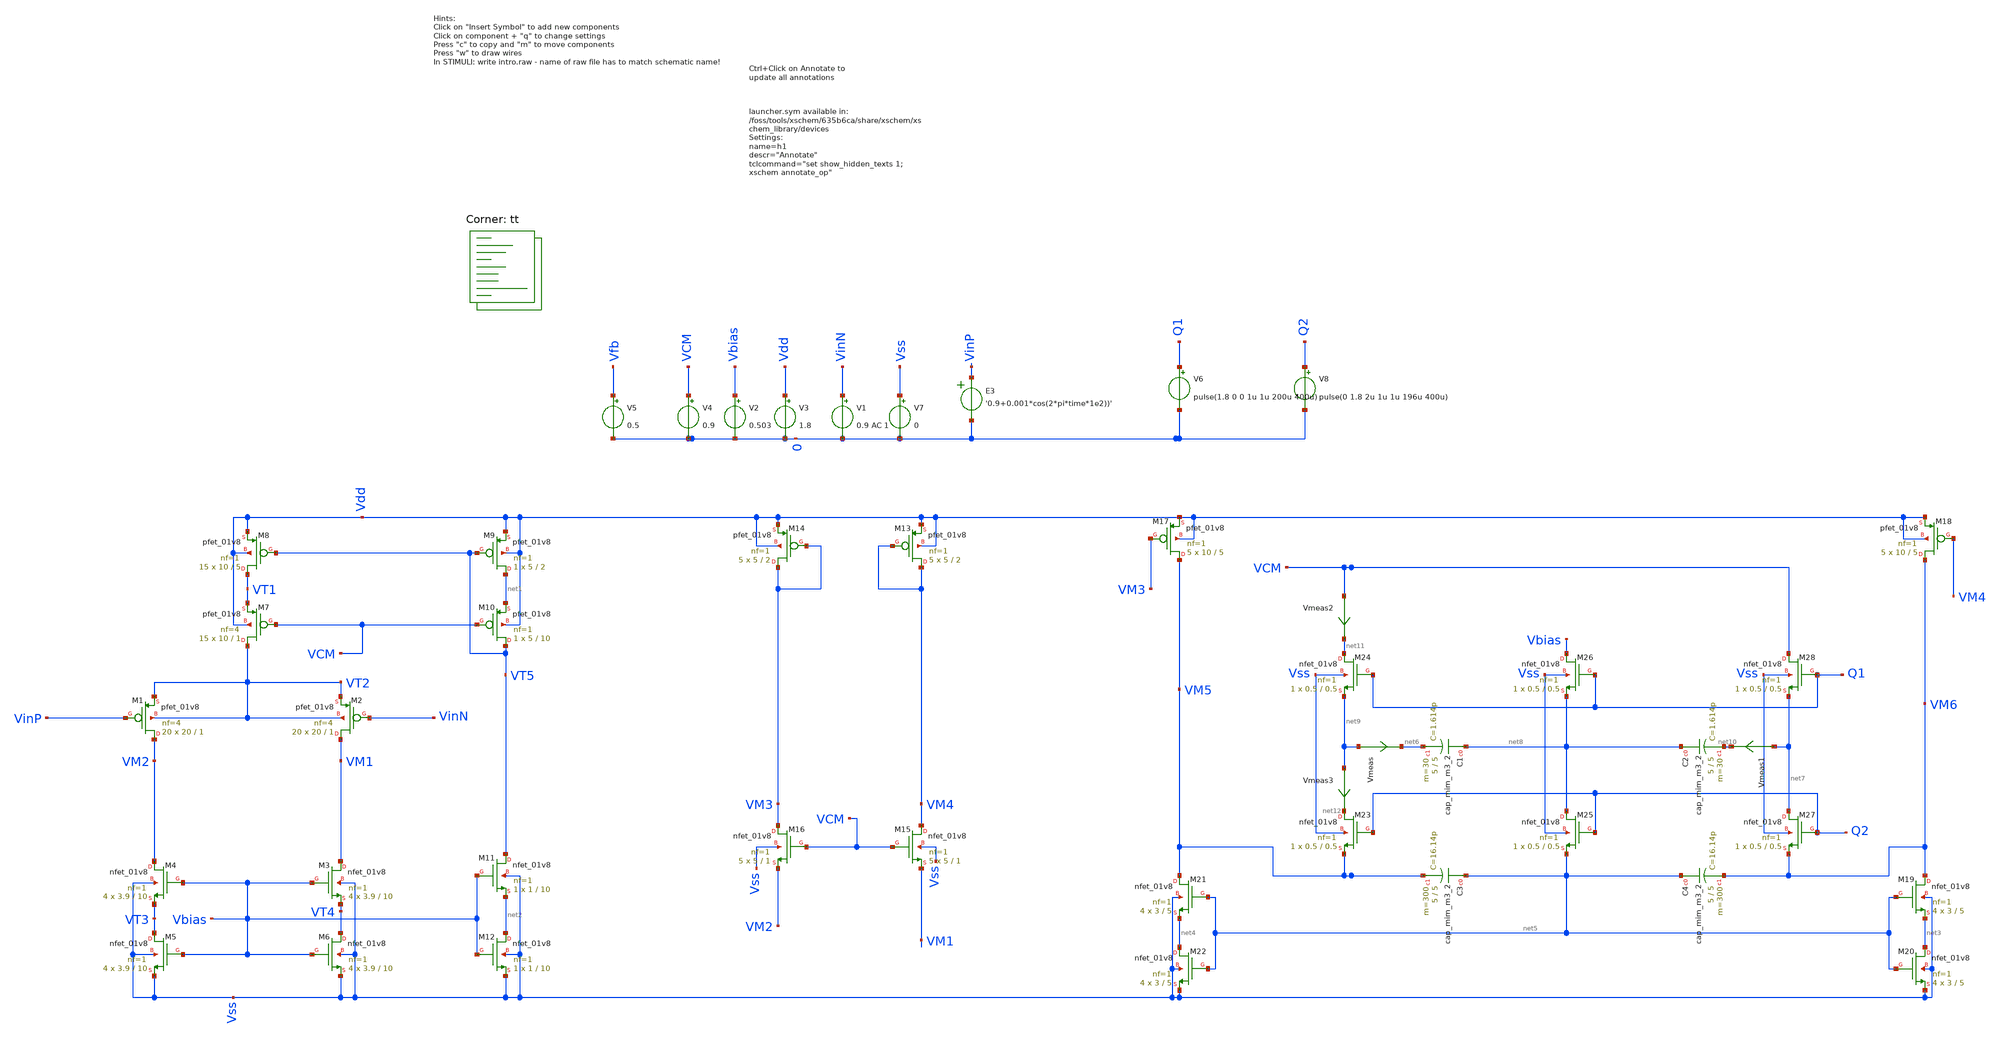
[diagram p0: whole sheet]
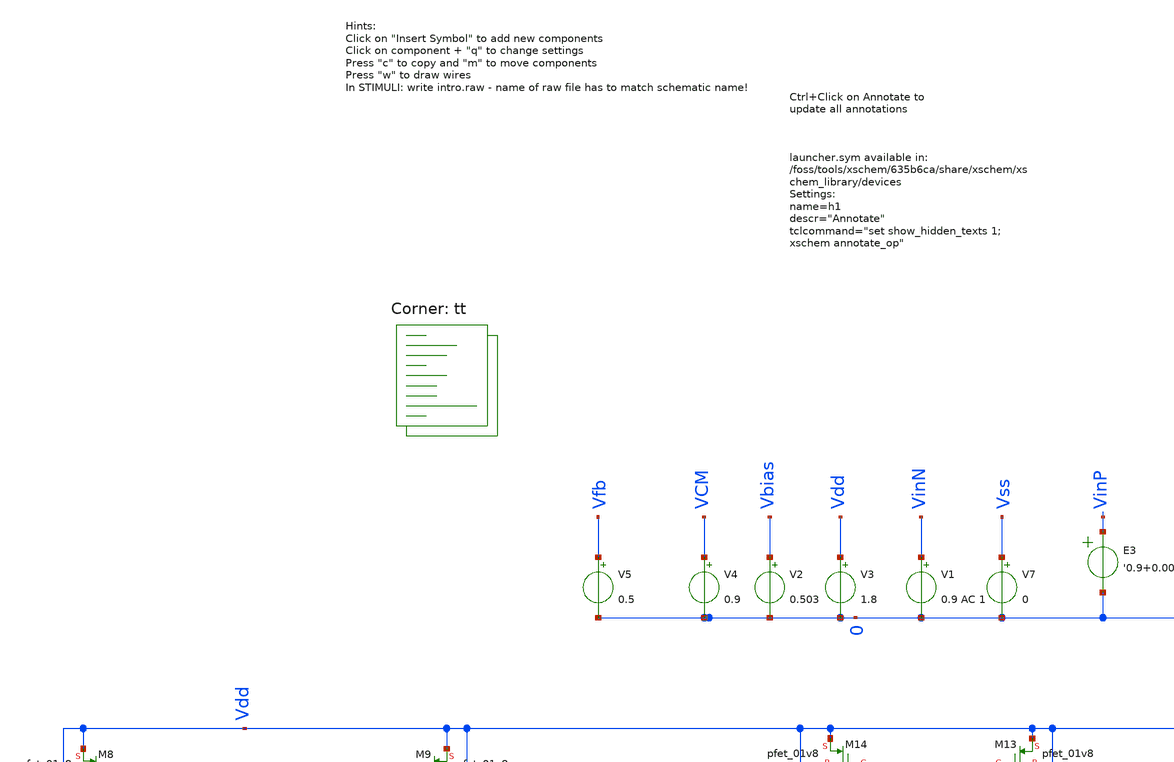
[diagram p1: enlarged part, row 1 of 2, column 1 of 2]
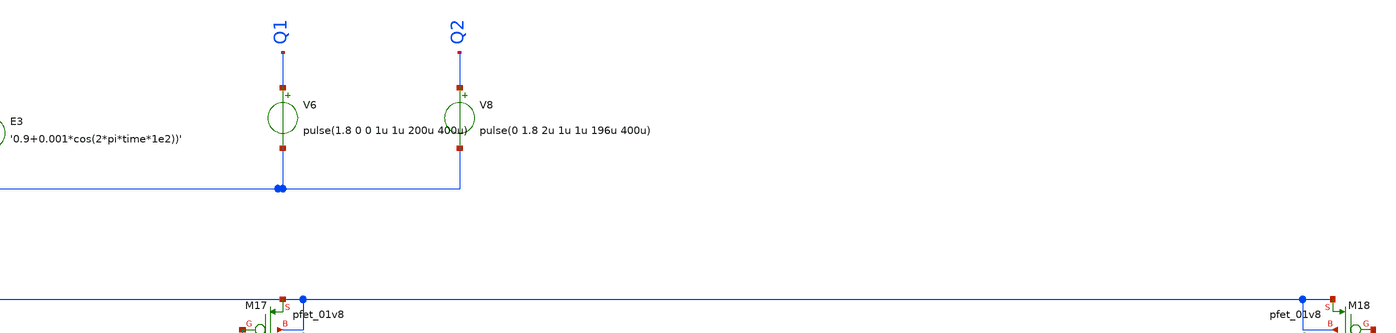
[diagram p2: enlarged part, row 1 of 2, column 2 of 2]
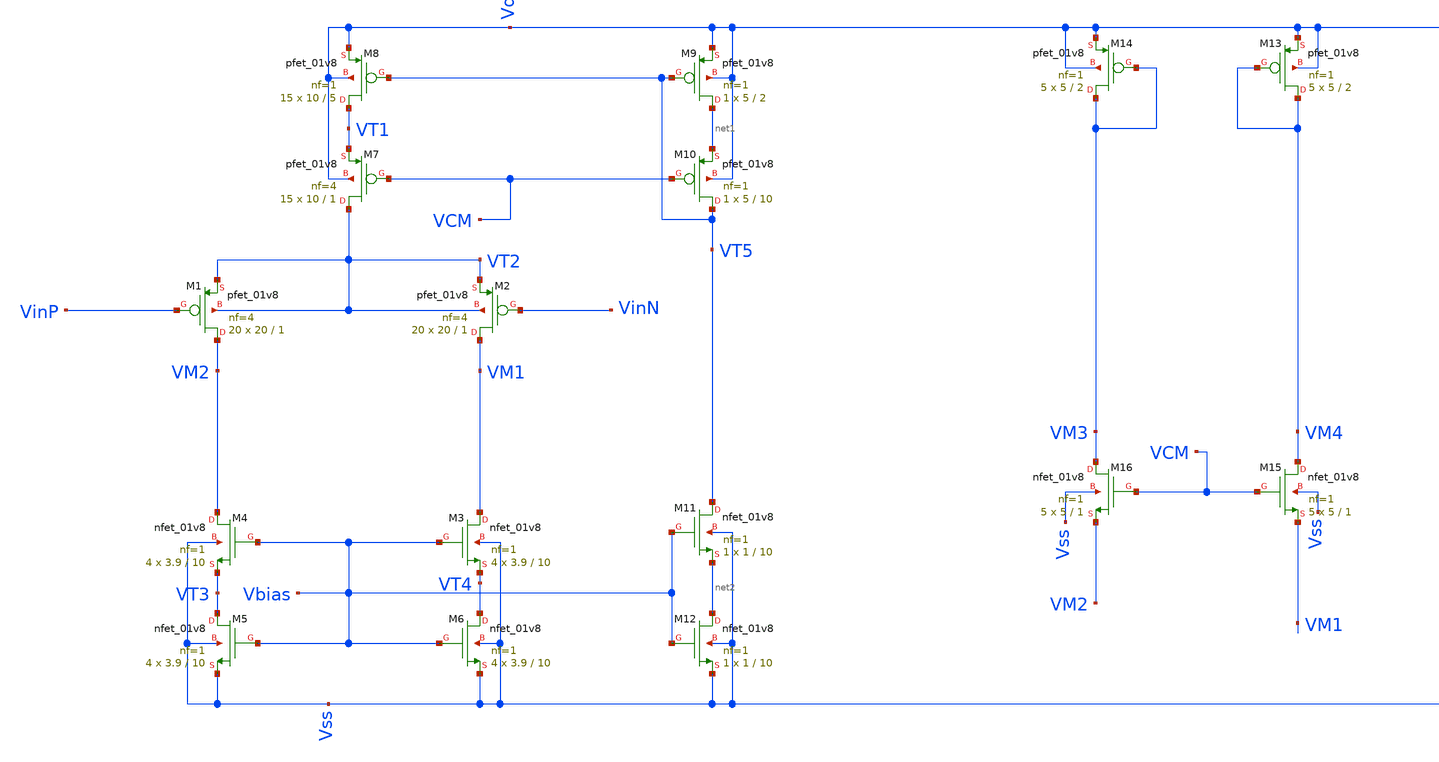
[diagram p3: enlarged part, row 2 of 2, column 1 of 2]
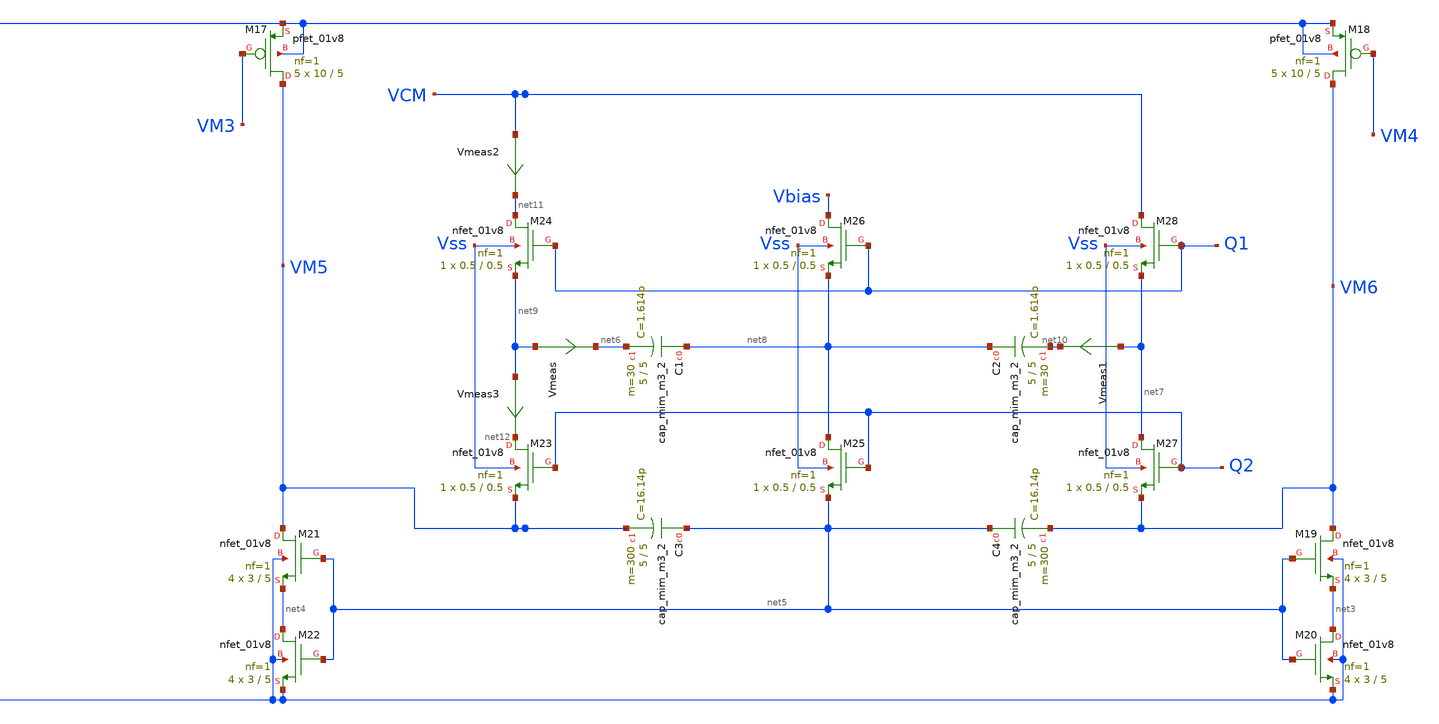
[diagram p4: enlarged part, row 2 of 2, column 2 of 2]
** sch_path: Backup1.sch
**.subckt Backup1
XM1 VM2 VinP VT2 VT2 sky130_fd_pr__pfet_01v8 L=1 W=20 nf=4 ad='int((nf+1)/2) * W/nf * 0.29' as='int((nf+2)/2) * W/nf * 0.29'
+ pd='2*int((nf+1)/2) * (W/nf + 0.29)' ps='2*int((nf+2)/2) * (W/nf + 0.29)' nrd='0.29 / W' nrs='0.29 / W'
+ sa=0 sb=0 sd=0 mult=20 m=20
XM2 VM1 VinN VT2 VT2 sky130_fd_pr__pfet_01v8 L=1 W=20 nf=4 ad='int((nf+1)/2) * W/nf * 0.29' as='int((nf+2)/2) * W/nf * 0.29'
+ pd='2*int((nf+1)/2) * (W/nf + 0.29)' ps='2*int((nf+2)/2) * (W/nf + 0.29)' nrd='0.29 / W' nrs='0.29 / W'
+ sa=0 sb=0 sd=0 mult=20 m=20
XM3 VM1 Vbias VT4 Vss sky130_fd_pr__nfet_01v8 L=10 W=3.9 nf=1 ad='int((nf+1)/2) * W/nf * 0.29' as='int((nf+2)/2) * W/nf * 0.29'
+ pd='2*int((nf+1)/2) * (W/nf + 0.29)' ps='2*int((nf+2)/2) * (W/nf + 0.29)' nrd='0.29 / W' nrs='0.29 / W'
+ sa=0 sb=0 sd=0 mult=4 m=4
XM4 VM2 Vbias VT3 Vss sky130_fd_pr__nfet_01v8 L=10 W=3.9 nf=1 ad='int((nf+1)/2) * W/nf * 0.29' as='int((nf+2)/2) * W/nf * 0.29'
+ pd='2*int((nf+1)/2) * (W/nf + 0.29)' ps='2*int((nf+2)/2) * (W/nf + 0.29)' nrd='0.29 / W' nrs='0.29 / W'
+ sa=0 sb=0 sd=0 mult=4 m=4
XM5 VT3 Vbias Vss Vss sky130_fd_pr__nfet_01v8 L=10 W=3.9 nf=1 ad='int((nf+1)/2) * W/nf * 0.29' as='int((nf+2)/2) * W/nf * 0.29'
+ pd='2*int((nf+1)/2) * (W/nf + 0.29)' ps='2*int((nf+2)/2) * (W/nf + 0.29)' nrd='0.29 / W' nrs='0.29 / W'
+ sa=0 sb=0 sd=0 mult=4 m=4
XM6 VT4 Vbias Vss Vss sky130_fd_pr__nfet_01v8 L=10 W=3.9 nf=1 ad='int((nf+1)/2) * W/nf * 0.29' as='int((nf+2)/2) * W/nf * 0.29'
+ pd='2*int((nf+1)/2) * (W/nf + 0.29)' ps='2*int((nf+2)/2) * (W/nf + 0.29)' nrd='0.29 / W' nrs='0.29 / W'
+ sa=0 sb=0 sd=0 mult=4 m=4
XM7 VT2 VCM VT1 Vdd sky130_fd_pr__pfet_01v8 L=1 W=10 nf=4 ad='int((nf+1)/2) * W/nf * 0.29' as='int((nf+2)/2) * W/nf * 0.29'
+ pd='2*int((nf+1)/2) * (W/nf + 0.29)' ps='2*int((nf+2)/2) * (W/nf + 0.29)' nrd='0.29 / W' nrs='0.29 / W'
+ sa=0 sb=0 sd=0 mult=15 m=15
XM8 VT1 VT5 Vdd Vdd sky130_fd_pr__pfet_01v8 L=5 W=10 nf=1 ad='int((nf+1)/2) * W/nf * 0.29' as='int((nf+2)/2) * W/nf * 0.29'
+ pd='2*int((nf+1)/2) * (W/nf + 0.29)' ps='2*int((nf+2)/2) * (W/nf + 0.29)' nrd='0.29 / W' nrs='0.29 / W'
+ sa=0 sb=0 sd=0 mult=15 m=15
XM9 net1 VT5 Vdd Vdd sky130_fd_pr__pfet_01v8 L=2 W=5 nf=1 ad='int((nf+1)/2) * W/nf * 0.29' as='int((nf+2)/2) * W/nf * 0.29'
+ pd='2*int((nf+1)/2) * (W/nf + 0.29)' ps='2*int((nf+2)/2) * (W/nf + 0.29)' nrd='0.29 / W' nrs='0.29 / W'
+ sa=0 sb=0 sd=0 mult=1 m=1
XM10 VT5 VCM net1 Vdd sky130_fd_pr__pfet_01v8 L=10 W=5 nf=1 ad='int((nf+1)/2) * W/nf * 0.29' as='int((nf+2)/2) * W/nf * 0.29'
+ pd='2*int((nf+1)/2) * (W/nf + 0.29)' ps='2*int((nf+2)/2) * (W/nf + 0.29)' nrd='0.29 / W' nrs='0.29 / W'
+ sa=0 sb=0 sd=0 mult=1 m=1
XM11 VT5 Vbias net2 Vss sky130_fd_pr__nfet_01v8 L=10 W=1 nf=1 ad='int((nf+1)/2) * W/nf * 0.29' as='int((nf+2)/2) * W/nf * 0.29'
+ pd='2*int((nf+1)/2) * (W/nf + 0.29)' ps='2*int((nf+2)/2) * (W/nf + 0.29)' nrd='0.29 / W' nrs='0.29 / W'
+ sa=0 sb=0 sd=0 mult=1 m=1
XM12 net2 Vbias Vss Vss sky130_fd_pr__nfet_01v8 L=10 W=1 nf=1 ad='int((nf+1)/2) * W/nf * 0.29' as='int((nf+2)/2) * W/nf * 0.29'
+ pd='2*int((nf+1)/2) * (W/nf + 0.29)' ps='2*int((nf+2)/2) * (W/nf + 0.29)' nrd='0.29 / W' nrs='0.29 / W'
+ sa=0 sb=0 sd=0 mult=1 m=1
XM13 VM4 VM4 Vdd Vdd sky130_fd_pr__pfet_01v8 L=2 W=5 nf=1 ad='int((nf+1)/2) * W/nf * 0.29' as='int((nf+2)/2) * W/nf * 0.29'
+ pd='2*int((nf+1)/2) * (W/nf + 0.29)' ps='2*int((nf+2)/2) * (W/nf + 0.29)' nrd='0.29 / W' nrs='0.29 / W'
+ sa=0 sb=0 sd=0 mult=5 m=5
XM14 VM3 VM3 Vdd Vdd sky130_fd_pr__pfet_01v8 L=2 W=5 nf=1 ad='int((nf+1)/2) * W/nf * 0.29' as='int((nf+2)/2) * W/nf * 0.29'
+ pd='2*int((nf+1)/2) * (W/nf + 0.29)' ps='2*int((nf+2)/2) * (W/nf + 0.29)' nrd='0.29 / W' nrs='0.29 / W'
+ sa=0 sb=0 sd=0 mult=5 m=5
XM15 VM4 VCM VM1 Vss sky130_fd_pr__nfet_01v8 L=1 W=5 nf=1 ad='int((nf+1)/2) * W/nf * 0.29' as='int((nf+2)/2) * W/nf * 0.29'
+ pd='2*int((nf+1)/2) * (W/nf + 0.29)' ps='2*int((nf+2)/2) * (W/nf + 0.29)' nrd='0.29 / W' nrs='0.29 / W'
+ sa=0 sb=0 sd=0 mult=5 m=5
XM16 VM3 VCM VM2 Vss sky130_fd_pr__nfet_01v8 L=1 W=5 nf=1 ad='int((nf+1)/2) * W/nf * 0.29' as='int((nf+2)/2) * W/nf * 0.29'
+ pd='2*int((nf+1)/2) * (W/nf + 0.29)' ps='2*int((nf+2)/2) * (W/nf + 0.29)' nrd='0.29 / W' nrs='0.29 / W'
+ sa=0 sb=0 sd=0 mult=5 m=5
XM17 VM5 VM3 Vdd Vdd sky130_fd_pr__pfet_01v8 L=5 W=10 nf=1 ad='int((nf+1)/2) * W/nf * 0.29' as='int((nf+2)/2) * W/nf * 0.29'
+ pd='2*int((nf+1)/2) * (W/nf + 0.29)' ps='2*int((nf+2)/2) * (W/nf + 0.29)' nrd='0.29 / W' nrs='0.29 / W'
+ sa=0 sb=0 sd=0 mult=5 m=5
XM18 VM6 VM4 Vdd Vdd sky130_fd_pr__pfet_01v8 L=5 W=10 nf=1 ad='int((nf+1)/2) * W/nf * 0.29' as='int((nf+2)/2) * W/nf * 0.29'
+ pd='2*int((nf+1)/2) * (W/nf + 0.29)' ps='2*int((nf+2)/2) * (W/nf + 0.29)' nrd='0.29 / W' nrs='0.29 / W'
+ sa=0 sb=0 sd=0 mult=5 m=5
XM19 VM6 net5 net3 Vss sky130_fd_pr__nfet_01v8 L=5 W=3 nf=1 ad='int((nf+1)/2) * W/nf * 0.29' as='int((nf+2)/2) * W/nf * 0.29'
+ pd='2*int((nf+1)/2) * (W/nf + 0.29)' ps='2*int((nf+2)/2) * (W/nf + 0.29)' nrd='0.29 / W' nrs='0.29 / W'
+ sa=0 sb=0 sd=0 mult=4 m=4
XM20 net3 net5 Vss Vss sky130_fd_pr__nfet_01v8 L=5 W=3 nf=1 ad='int((nf+1)/2) * W/nf * 0.29' as='int((nf+2)/2) * W/nf * 0.29'
+ pd='2*int((nf+1)/2) * (W/nf + 0.29)' ps='2*int((nf+2)/2) * (W/nf + 0.29)' nrd='0.29 / W' nrs='0.29 / W'
+ sa=0 sb=0 sd=0 mult=4 m=4
XM21 VM5 net5 net4 Vss sky130_fd_pr__nfet_01v8 L=5 W=3 nf=1 ad='int((nf+1)/2) * W/nf * 0.29' as='int((nf+2)/2) * W/nf * 0.29'
+ pd='2*int((nf+1)/2) * (W/nf + 0.29)' ps='2*int((nf+2)/2) * (W/nf + 0.29)' nrd='0.29 / W' nrs='0.29 / W'
+ sa=0 sb=0 sd=0 mult=4 m=4
XM22 net4 net5 Vss Vss sky130_fd_pr__nfet_01v8 L=5 W=3 nf=1 ad='int((nf+1)/2) * W/nf * 0.29' as='int((nf+2)/2) * W/nf * 0.29'
+ pd='2*int((nf+1)/2) * (W/nf + 0.29)' ps='2*int((nf+2)/2) * (W/nf + 0.29)' nrd='0.29 / W' nrs='0.29 / W'
+ sa=0 sb=0 sd=0 mult=4 m=4
E3 VinP 0 VOL=' '0.9+0.001*cos(2*pi*time*1e2))' '
V3 Vdd 0 1.8
V7 Vss 0 0
V1 VinN 0 0.9 AC 1
V2 Vbias 0 0.503
V4 VCM 0 0.9
V5 Vfb 0 0.5
XC1 net8 net6 sky130_fd_pr__cap_mim_m3_2 W=5 L=5 MF=30 m=30
XC2 net8 net10 sky130_fd_pr__cap_mim_m3_2 W=5 L=5 MF=30 m=30
XC3 net5 VM5 sky130_fd_pr__cap_mim_m3_2 W=5 L=5 MF=300 m=300
XC4 net5 VM6 sky130_fd_pr__cap_mim_m3_2 W=5 L=5 MF=300 m=300
XM23 net12 Q2 VM5 Vss sky130_fd_pr__nfet_01v8 L=0.5 W=0.5 nf=1 ad='int((nf+1)/2) * W/nf * 0.29' as='int((nf+2)/2) * W/nf * 0.29'
+ pd='2*int((nf+1)/2) * (W/nf + 0.29)' ps='2*int((nf+2)/2) * (W/nf + 0.29)' nrd='0.29 / W' nrs='0.29 / W'
+ sa=0 sb=0 sd=0 mult=1 m=1
XM24 net11 Q1 net9 Vss sky130_fd_pr__nfet_01v8 L=0.5 W=0.5 nf=1 ad='int((nf+1)/2) * W/nf * 0.29' as='int((nf+2)/2) * W/nf * 0.29'
+ pd='2*int((nf+1)/2) * (W/nf + 0.29)' ps='2*int((nf+2)/2) * (W/nf + 0.29)' nrd='0.29 / W' nrs='0.29 / W'
+ sa=0 sb=0 sd=0 mult=1 m=1
XM25 net8 Q2 net5 Vss sky130_fd_pr__nfet_01v8 L=0.5 W=0.5 nf=1 ad='int((nf+1)/2) * W/nf * 0.29' as='int((nf+2)/2) * W/nf * 0.29'
+ pd='2*int((nf+1)/2) * (W/nf + 0.29)' ps='2*int((nf+2)/2) * (W/nf + 0.29)' nrd='0.29 / W' nrs='0.29 / W'
+ sa=0 sb=0 sd=0 mult=1 m=1
XM26 Vbias Q1 net8 Vss sky130_fd_pr__nfet_01v8 L=0.5 W=0.5 nf=1 ad='int((nf+1)/2) * W/nf * 0.29' as='int((nf+2)/2) * W/nf * 0.29'
+ pd='2*int((nf+1)/2) * (W/nf + 0.29)' ps='2*int((nf+2)/2) * (W/nf + 0.29)' nrd='0.29 / W' nrs='0.29 / W'
+ sa=0 sb=0 sd=0 mult=1 m=1
XM27 net7 Q2 VM6 Vss sky130_fd_pr__nfet_01v8 L=0.5 W=0.5 nf=1 ad='int((nf+1)/2) * W/nf * 0.29' as='int((nf+2)/2) * W/nf * 0.29'
+ pd='2*int((nf+1)/2) * (W/nf + 0.29)' ps='2*int((nf+2)/2) * (W/nf + 0.29)' nrd='0.29 / W' nrs='0.29 / W'
+ sa=0 sb=0 sd=0 mult=1 m=1
XM28 VCM Q1 net7 Vss sky130_fd_pr__nfet_01v8 L=0.5 W=0.5 nf=1 ad='int((nf+1)/2) * W/nf * 0.29' as='int((nf+2)/2) * W/nf * 0.29'
+ pd='2*int((nf+1)/2) * (W/nf + 0.29)' ps='2*int((nf+2)/2) * (W/nf + 0.29)' nrd='0.29 / W' nrs='0.29 / W'
+ sa=0 sb=0 sd=0 mult=1 m=1
V6 Q1 0 pulse(1.8 0 0 1u 1u 200u 400u)
V8 Q2 0 pulse(0 1.8 2u 1u 1u 196u 400u)
Vmeas net9 net6 0
.save i(vmeas)
Vmeas1 net7 net10 0
.save i(vmeas1)
Vmeas2 VCM net11 0
.save i(vmeas2)
Vmeas3 net9 net12 0
.save i(vmeas3)
**** begin user architecture code


.options savecurrents
.control



save all
save @m.xm1.msky130_fd_pr__nfet_01v8_lvt[id]
save @m.xm1.msky130_fd_pr__pfet_01v8[id]
save @m.xm7.msky130_fd_pr__pfet_01v8[id]
save @m.xm1.msky130_fd_pr__nfet_01v8_lvt[vth]
save @m.xm1.msky130_fd_pr__nfet_01v8_lvt[vgs]
save @m.xm1.msky130_fd_pr__nfet_01v8_lvt[vds]
save @m.xm1.msky130_fd_pr__nfet_01v8_lvt[gm]
save @m.xm1.msky130_fd_pr__nfet_01v8_lvt[gds]
save @m.xm23.msky130_fd_pr__nfet_01v8[cgs]
save @m.xm15.msky130_fd_pr__nfet_01v8[cgs]

save @m.xm1.msky130_fd_pr__pfet_01v8[id]
save @m.xm2.msky130_fd_pr__pfet_01v8_lvt[id]
save @m.xm2.msky130_fd_pr__pfet_01v8_lvt[vth]
save @m.xm1.msky130_fd_pr__pfet_01v8[vgs]
save @m.xm2.msky130_fd_pr__pfet_01v8_lvt[vds]
save @m.xm2.msky130_fd_pr__pfet_01v8_lvt[gm]
save @m.xm2.msky130_fd_pr__pfet_01v8_lvt[gds]
save @m.xm2.msky130_fd_pr__pfet_01v8_lvt[cgs]

op
remzerovec
write intro.raw
*set appendwrite

*dc V1 0 1.8 0.01
*plot @m.xm1.msky130_fd_pr__nfet_01v8_lvt[id] @m.xm2.msky130_fd_pr__pfet_01v8_lvt[id]
*remzerovec
*write intro.raw

.endc
.control
tran 0.1u 50m
save all
plot v(VM5)
plot v(VM5)-v(VM6)

*noise V(VM5,VM6) V1 dec 100 0.1 100
*print inoise_total onoise_total
*setplot noise1
*plot inoise_spectrum

.endc





.lib $::SKYWATER_MODELS/sky130.lib.spice tt
**** end user architecture code
**.ends
.end
